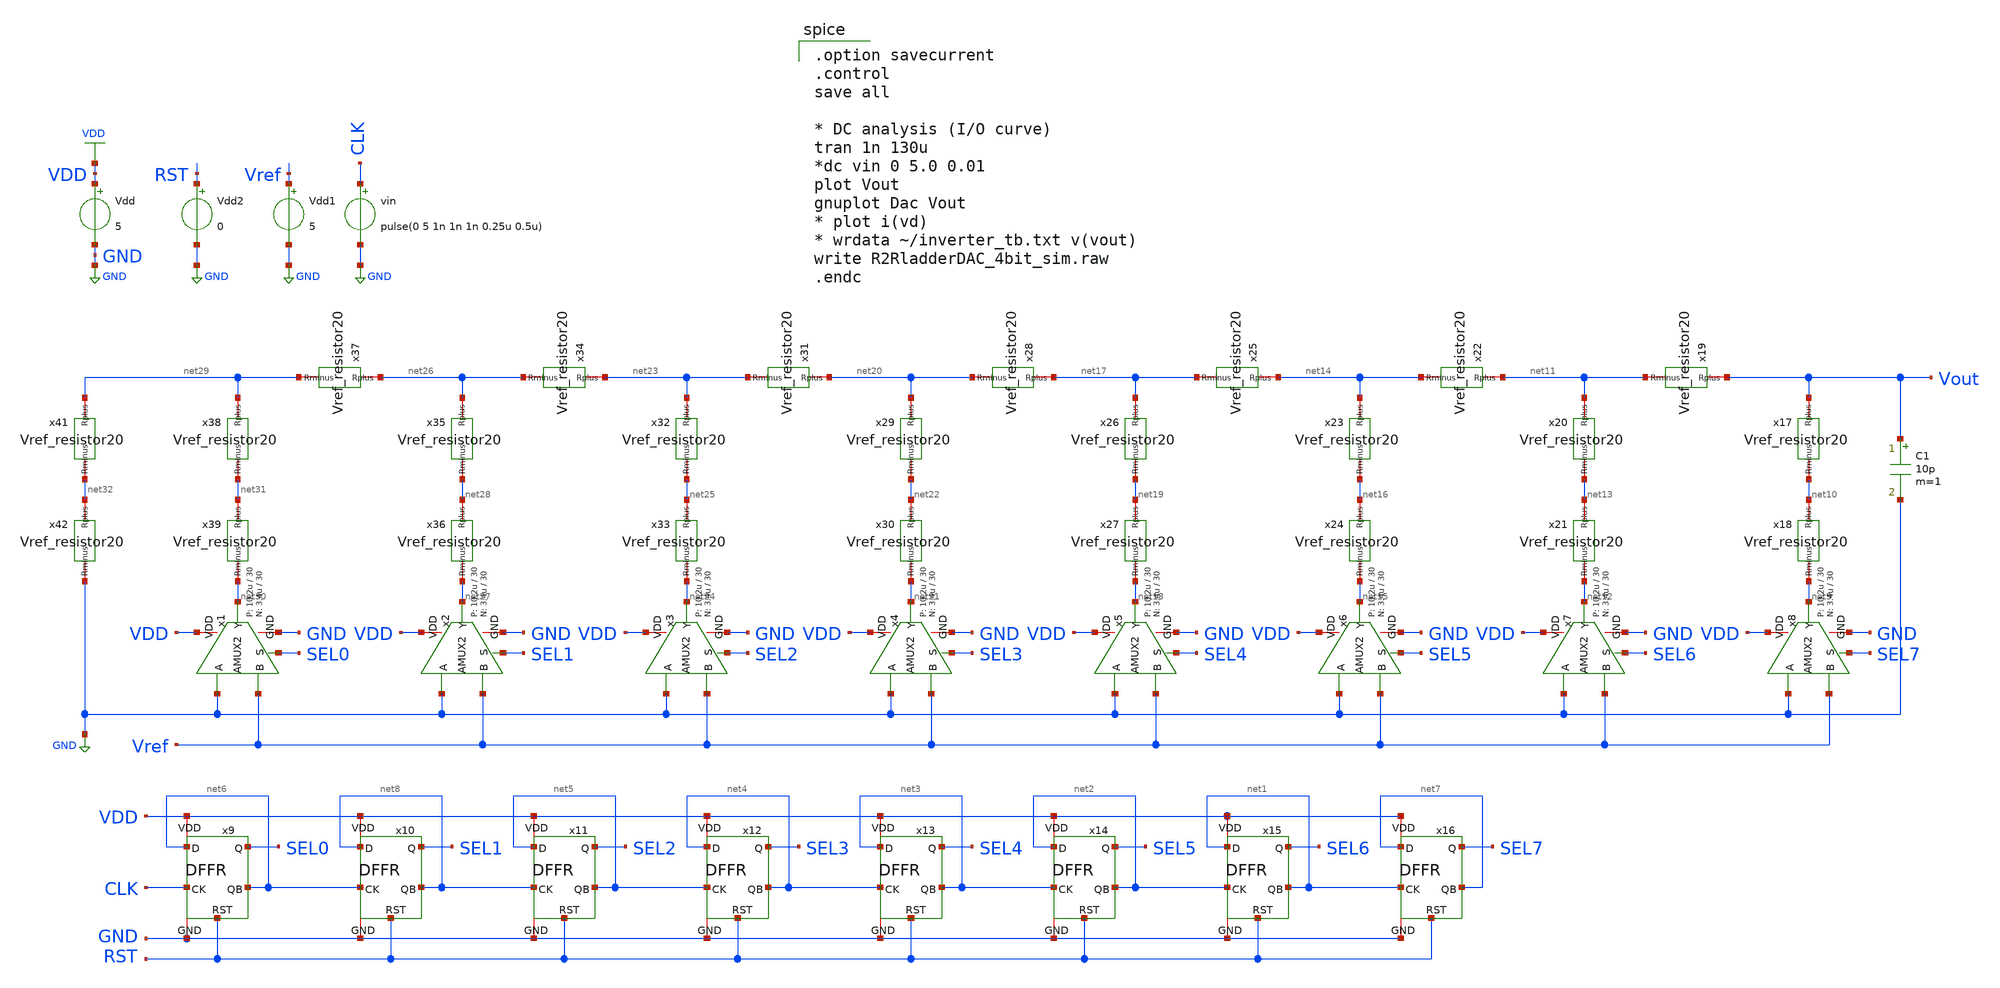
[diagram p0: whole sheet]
** sch_path: Vol.2/files/05/xschem/R2RladderDAC_8bit_sim.sch
**.subckt R2RladderDAC_8bit_sim
Vdd VDD GND 5
Vdd1 Vref GND 5
vin CLK GND pulse(0 5 1n 1n 1n 0.25u 0.5u)
x9 VDD net6 net6 SEL0 RST GND CLK DFFR
x10 VDD net8 net8 SEL1 RST GND net6 DFFR
x11 VDD net5 net5 SEL2 RST GND net8 DFFR
x12 VDD net4 net4 SEL3 RST GND net5 DFFR
x13 VDD net3 net3 SEL4 RST GND net4 DFFR
x14 VDD net2 net2 SEL5 RST GND net3 DFFR
x15 VDD net1 net1 SEL6 RST GND net2 DFFR
x16 VDD net7 net7 SEL7 RST GND net1 DFFR
Vdd2 RST GND 0
x17 Vout net10 Vref_resistor20
x18 net10 net9 Vref_resistor20
x19 Vout net11 Vref_resistor20
x20 net11 net13 Vref_resistor20
x21 net13 net12 Vref_resistor20
x22 net11 net14 Vref_resistor20
x23 net14 net16 Vref_resistor20
x24 net16 net15 Vref_resistor20
x25 net14 net17 Vref_resistor20
x26 net17 net19 Vref_resistor20
x27 net19 net18 Vref_resistor20
x28 net17 net20 Vref_resistor20
x29 net20 net22 Vref_resistor20
x30 net22 net21 Vref_resistor20
x31 net20 net23 Vref_resistor20
x32 net23 net25 Vref_resistor20
x33 net25 net24 Vref_resistor20
x34 net23 net26 Vref_resistor20
x35 net26 net28 Vref_resistor20
x36 net28 net27 Vref_resistor20
x37 net26 net29 Vref_resistor20
x38 net29 net31 Vref_resistor20
x39 net31 net30 Vref_resistor20
x41 net29 net32 Vref_resistor20
x42 net32 GND Vref_resistor20
x1 VDD Vref net30 SEL0 GND GND AMUX2 WP=10.2u WPM=30 WN=3.4u WNM=30
x2 VDD Vref net27 SEL1 GND GND AMUX2 WP=10.2u WPM=30 WN=3.4u WNM=30
x3 VDD Vref net24 SEL2 GND GND AMUX2 WP=10.2u WPM=30 WN=3.4u WNM=30
x4 VDD Vref net21 SEL3 GND GND AMUX2 WP=10.2u WPM=30 WN=3.4u WNM=30
x5 VDD Vref net18 SEL4 GND GND AMUX2 WP=10.2u WPM=30 WN=3.4u WNM=30
x6 VDD Vref net15 SEL5 GND GND AMUX2 WP=10.2u WPM=30 WN=3.4u WNM=30
x7 VDD Vref net12 SEL6 GND GND AMUX2 WP=10.2u WPM=30 WN=3.4u WNM=30
x8 VDD Vref net9 SEL7 GND GND AMUX2 WP=10.2u WPM=30 WN=3.4u WNM=30
C1 Vout GND 10p m=1
**** begin user architecture code
 .include $::LIB/../ip62_models

.option savecurrent
.control
save all

* DC analysis (I/O curve)
tran 1n 130u
*dc vin 0 5.0 0.01
plot Vout
gnuplot Dac Vout
* plot i(vd)
* wrdata ~/inverter_tb.txt v(vout)
write R2RladderDAC_4bit_sim.raw
.endc

**** end user architecture code
**.ends
.GLOBAL GND
.GLOBAL VDD
.end
